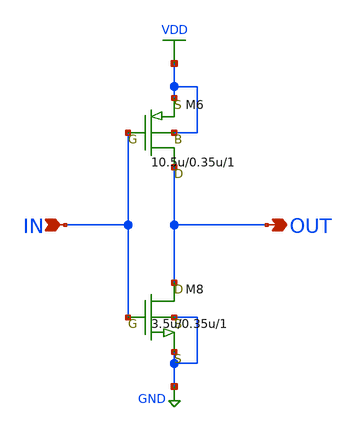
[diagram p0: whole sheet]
** sch_path: LR_hokari/LR_Work2/symbol/INVERTER.sch
**.subckt INVERTER OUT IN
*.opin OUT
*.ipin IN
M6 OUT IN VDD VDD pch w=10.5u l=0.35u as=0 ps=0 ad=0 pd=0 m=1
M8 OUT IN GND GND nch w=3.5u l=0.35u as=0 ps=0 ad=0 pd=0 m=1
**.ends
.GLOBAL VDD
.GLOBAL GND
.end
